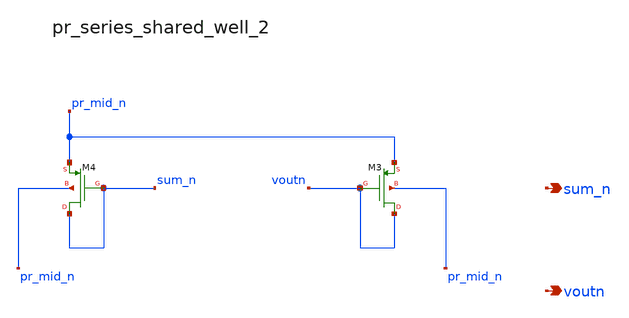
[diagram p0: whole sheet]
** sch_path: analog-db/raw/ia_005_hsu_pga_ideal/hier/blocks/pr_series_shared_well_2.sch
**.subckt pr_series_shared_well_2 sum_n voutn
*.opin sum_n
*.opin voutn
XM3 voutn voutn pr_mid_n pr_mid_n sg13_lv_pmos w=x_dut_xm3_w l=x_dut_xm3_l ng=1 m=x_dut_xm3_m
XM4 sum_n sum_n pr_mid_n pr_mid_n sg13_lv_pmos w=x_dut_xm4_w l=x_dut_xm4_l ng=1 m=x_dut_xm4_m
**.ends
.end
